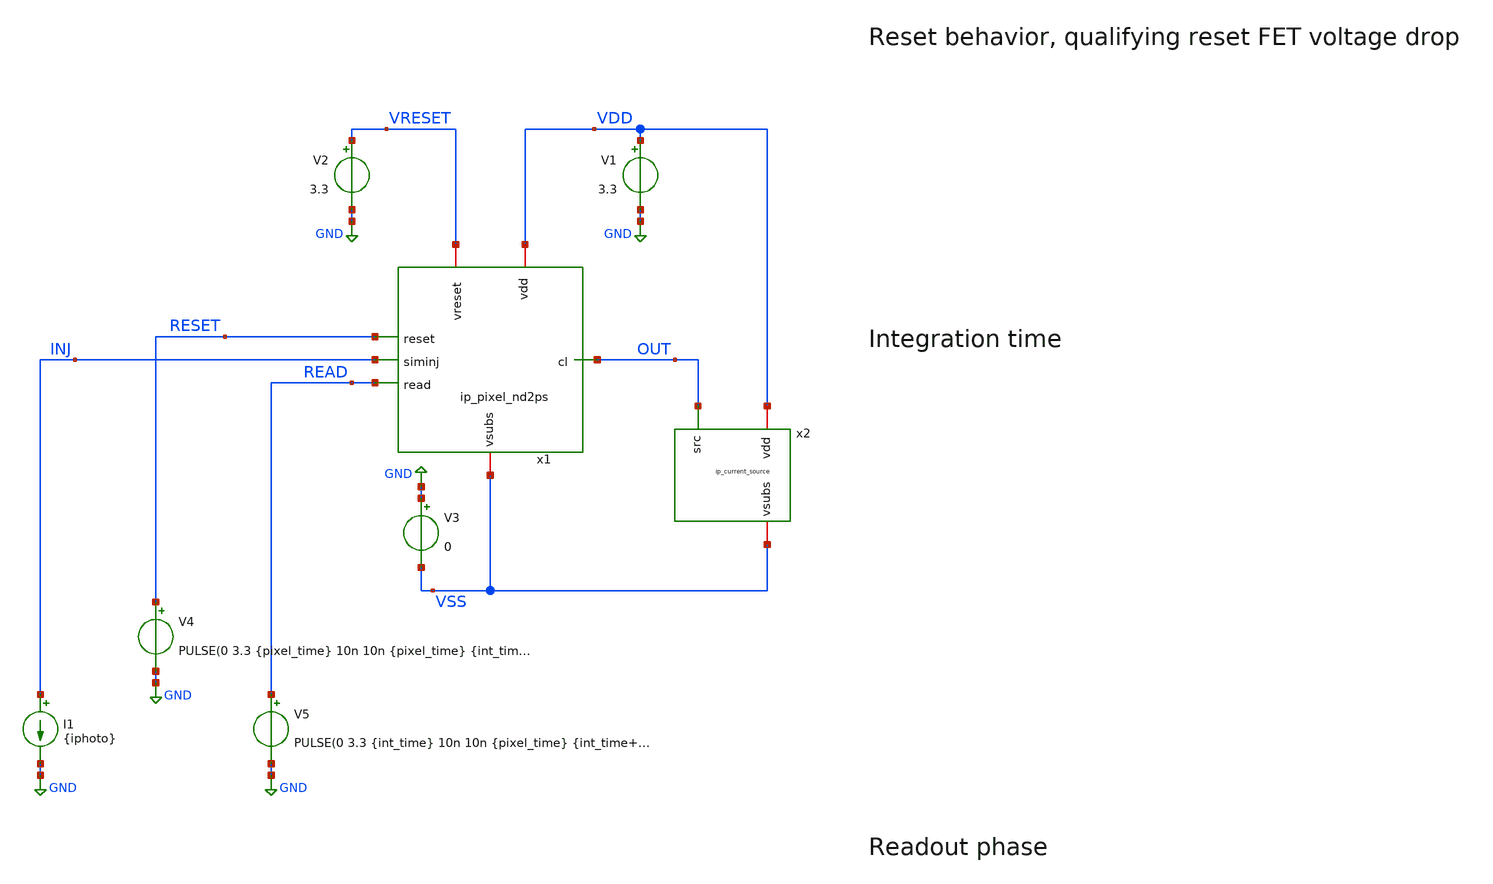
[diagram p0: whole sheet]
** sch_path: xschem/tb_pixel_nd2ps_tran.sch
**.subckt tb_pixel_nd2ps_tran
V1 VDD GND 3.3
V2 VRESET GND 3.3
V3 GND VSS 0
I1 INJ GND {iphoto}
V4 RESET GND PULSE(0 3.3 {pixel_time} 10n 10n {pixel_time} {int_time+10*pixel_time})
V5 READ GND PULSE(0 3.3 {int_time} 10n 10n {pixel_time} {int_time+10*pixel_time})
x2 VDD OUT VSS ip_current_source
x1 VDD VRESET RESET INJ OUT READ VSS ip_pixel_nd2ps
**** begin user architecture code

.include $::180MCU_MODELS/design.ngspice
.lib $::180MCU_MODELS/sm141064.ngspice typical
.lib $::180MCU_MODELS/sm141064.ngspice res_typical
.lib $::180MCU_MODELS/sm141064.ngspice moscap_typical
.lib $::180MCU_MODELS/sm141064.ngspice diode_typical
* .lib $::180MCU_MODELS/sm141064.ngspice res_statistical




.param pixel_time=10u
.param int_time=1m
.param iphoto=10p
.control
	shell rm -f tb_pixel_nd2ps_tran.raw
	set appendwrite
	foreach iphoto 0f 10f 100f 1p 10p 100p
		alterparam iphoto = $iphoto
		reset
		op
		tran 25n 2.2m
		save all
		write tb_pixel_nd2ps_tran.raw
	end
	quit
.endc



**** end user architecture code
**.ends

* expanding   symbol:  ip_current_source.sym # of pins=3
** sym_path: xschem/ip_current_source.sym
** sch_path: xschem/ip_current_source.sch
.subckt ip_current_source vdd src vsubs
*.iopin vdd
*.iopin vsubs
*.ipin src
XM1 net1 net1 vsubs vsubs nfet_03v3 L=1u W=3u nf=1 ad='int((nf+1)/2) * W/nf * 0.18u' as='int((nf+2)/2) * W/nf * 0.18u'
+ pd='2*int((nf+1)/2) * (W/nf + 0.18u)' ps='2*int((nf+2)/2) * (W/nf + 0.18u)' nrd='0.18u / W' nrs='0.18u / W'
+ sa=0 sb=0 sd=0 m=1
XM2 net2 net1 vsubs vsubs nfet_03v3 L=10u W=0.3u nf=1 ad='int((nf+1)/2) * W/nf * 0.18u' as='int((nf+2)/2) * W/nf * 0.18u'
+ pd='2*int((nf+1)/2) * (W/nf + 0.18u)' ps='2*int((nf+2)/2) * (W/nf + 0.18u)' nrd='0.18u / W' nrs='0.18u / W'
+ sa=0 sb=0 sd=0 m=1
XR2 vdd net1 vsubs ppolyf_u_3k r_width=1e-6 r_length=6e-6 m=1
XM3 src net1 net2 vsubs nfet_03v3 L=0.3u W=10u nf=1 ad='int((nf+1)/2) * W/nf * 0.18u' as='int((nf+2)/2) * W/nf * 0.18u'
+ pd='2*int((nf+1)/2) * (W/nf + 0.18u)' ps='2*int((nf+2)/2) * (W/nf + 0.18u)' nrd='0.18u / W' nrs='0.18u / W'
+ sa=0 sb=0 sd=0 m=1
.ends


* expanding   symbol:  ip_pixel_nd2ps.sym # of pins=7
** sym_path: xschem/ip_pixel_nd2ps.sym
** sch_path: xschem/ip_pixel_nd2ps.sch
.subckt ip_pixel_nd2ps vdd vreset reset siminj cl read vsubs
*.iopin vdd
*.iopin vsubs
*.ipin siminj
*.ipin reset
*.ipin read
*.iopin vreset
*.opin cl
XM1 vreset reset siminj vsubs nfet_03v3 L=0.3u W=0.3u nf=1 ad='int((nf+1)/2) * W/nf * 0.18u' as='int((nf+2)/2) * W/nf * 0.18u'
+ pd='2*int((nf+1)/2) * (W/nf + 0.18u)' ps='2*int((nf+2)/2) * (W/nf + 0.18u)' nrd='0.18u / W' nrs='0.18u / W'
+ sa=0 sb=0 sd=0 m=1
XM2 vdd siminj sfout vsubs nfet_03v3 L=0.3u W=0.3u nf=1 ad='int((nf+1)/2) * W/nf * 0.18u' as='int((nf+2)/2) * W/nf * 0.18u'
+ pd='2*int((nf+1)/2) * (W/nf + 0.18u)' ps='2*int((nf+2)/2) * (W/nf + 0.18u)' nrd='0.18u / W' nrs='0.18u / W'
+ sa=0 sb=0 sd=0 m=1
XM3 sfout read cl vsubs nfet_03v3 L=0.3u W=1u nf=1 ad='int((nf+1)/2) * W/nf * 0.18u' as='int((nf+2)/2) * W/nf * 0.18u'
+ pd='2*int((nf+1)/2) * (W/nf + 0.18u)' ps='2*int((nf+2)/2) * (W/nf + 0.18u)' nrd='0.18u / W' nrs='0.18u / W'
+ sa=0 sb=0 sd=0 m=1
D1 vsubs siminj diode_nd2ps_03v3 area='12u * 10u ' pj='2*12u + 2*10u ' m=1
.ends

.GLOBAL GND
.end
